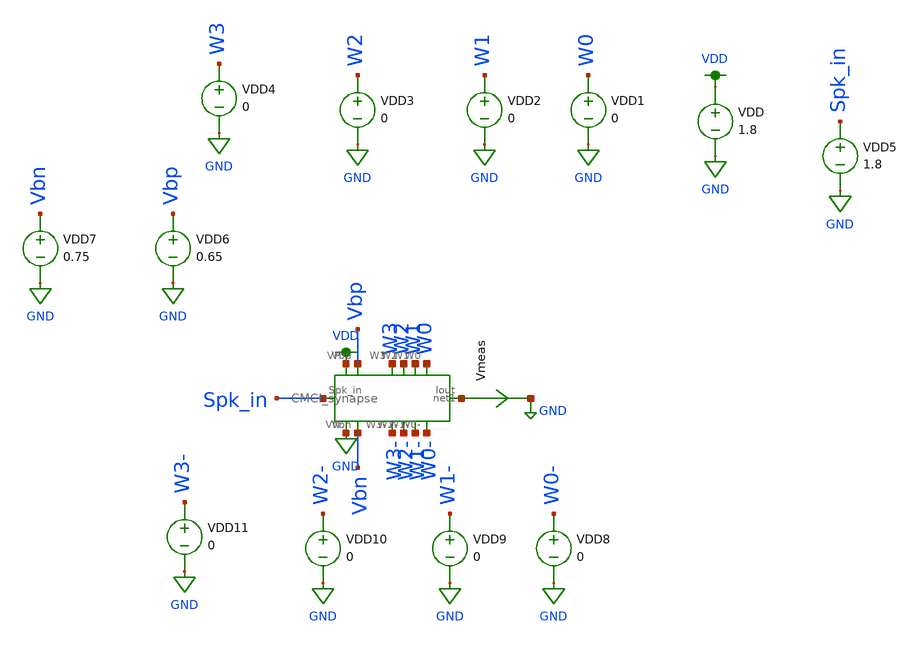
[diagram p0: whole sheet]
** sch_path: schematic/tran_CMCI.sch
**.subckt tran_CMCI
VDD VDD GND 1.8
VDD1 W0 GND 0
VDD2 W1 GND 0
VDD3 W2 GND 0
VDD4 W3 GND 0
VDD5 Spk_in GND 1.8
VDD6 Vbp GND 0.65
VDD7 Vbn GND 0.75
X1 VDD Vbp W3 W2 W1 W0 net1 W0- W1- W2- W3- Vbn GND Spk_in CMCI_synapse
VDD8 W0- GND 0
VDD9 W1- GND 0
VDD10 W2- GND 0
VDD11 W3- GND 0
Vmeas net1 GND 0
.save i(vmeas)
**** begin user architecture code

.param W=12
.param L=0.5
.control
set wr_vecnames
set wr_singlescale
let code = 0
  while code < 16
    if code eq 0
      let W0- = 0
    else
      let W0- = code % 2 * 1.8
    end
    if floor(code / 2) eq 0
      let W1- = 0
    else
      let W1- = floor(code / 2) % 2 * 1.8
    end
    if floor(code / 4) eq 0
      let W2- = 0
    else
      let W2- = floor(code / 4) % 2 * 1.8
    end
    if floor(code / 8) eq 0
      let W3- = 0
    else
      let W3- = floor(code / 8) % 2 * 1.8
    end
    alter vdd8 $&w0-
    alter vdd9 $&w1-
    alter vdd10 $&w2-
    alter vdd11 $&w3-
    save all
    op
    wrdata ~/neuromorphic_computing_final/dac_sim.txt i(Vmeas) v(W3-) v(W2-) v(W1-) v(W0-)
    if code eq 0
      set appendwrite
      set wr_vecnames = FALSE
    end
    let code = code + 1
  end
.endc


.option wnflag=1
.param MC_SWITCH=0.0
.lib ~/skywater/skywater-pdk/libraries/sky130_fd_pr_ngspice/latest/models/sky130.lib.spice tt

**** end user architecture code
**.ends
.GLOBAL VDD
.GLOBAL GND
.end
